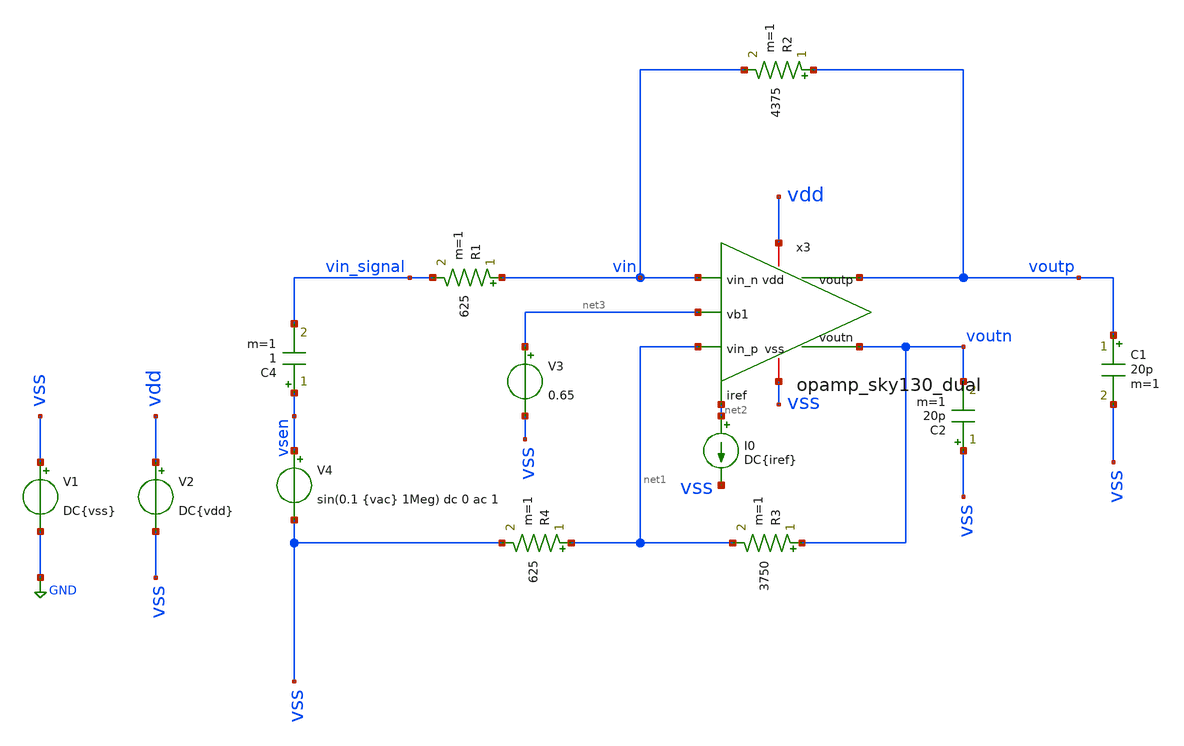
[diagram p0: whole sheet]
** sch_path: sch/tb_opamp_sky130_dual.sch
**.subckt tb_opamp_sky130_dual
V1 vss GND DC{vss}
V2 vdd vss DC{vdd}
V4 vsen vss sin(0.1 {vac} 1Meg) dc 0 ac 1
C4 vsen vin_signal 1 m=1
I0 net2 vss DC{iref}
R1 vin vin_signal 625 m=1
C1 voutp vss 20p m=1
R2 voutp vin 4375 m=1
C2 vss voutn 20p m=1
x3 vdd net2 vin net1 voutn voutp net3 vss opamp_sky130_dual
R3 voutn net1 3750 m=1
R4 net1 vss 625 m=1
V3 net3 vss 0.65
**** begin user architecture code




* Circuit Parameters
.param iref = 100u
.param vdd  = 1.8
.param vss  = 0.0
.param vac  = 0.1
.param vcm  = 0.7
.options TEMP = 65.0

* Include Models
*.lib ~/skywater_pdk/skywater-pdk/libraries/sky130_fd_pr/latest/models/corners/sky130.lib TT

* OP Parameters & Singals to save
.save all

*Simulations
.control


  reset
  tran 0.01u 11u
  setplot tran1
  plot v(vsen)  v(voutp) v(voutn)
  write tb_opamp_sky130_dual.raw

.endc

.end



** opencircuitdesign pdks install
.lib $::SKYWATER_MODELS/sky130.lib.spice tt


**** end user architecture code
**.ends

* expanding   symbol:  /home/alex/Desktop/EDA/TIA_IPN/sch/opamp_sky130_dual.sym # of pins=8
** sym_path: sch/opamp_sky130_dual.sym
** sch_path: sch/opamp_sky130_dual.sch
.subckt opamp_sky130_dual vdd iref vin_n vin_p voutn voutp vb1 vss
*.iopin vdd
*.iopin vss
*.ipin vin_n
*.ipin vin_p
*.ipin iref
*.opin voutn
*.opin voutp
*.ipin vb1
XM1 voe2 vin_n vp vp sky130_fd_pr__pfet_01v8 L=0.3 W=3 nf=1 ad='W * 0.29' as='W * 0.29' pd='2 * (W + 0.29)'
+ ps='2 * (W + 0.29)' nrd='0.29 / W' nrs='0.29 / W' sa=0 sb=0 sd=0 mult=200 m=200
XM2 voe1 vin_p vp vp sky130_fd_pr__pfet_01v8 L=0.3 W=3 nf=1 ad='W * 0.29' as='W * 0.29' pd='2 * (W + 0.29)'
+ ps='2 * (W + 0.29)' nrd='0.29 / W' nrs='0.29 / W' sa=0 sb=0 sd=0 mult=200 m=200
XM3 voe2 vb1 vss vss sky130_fd_pr__nfet_01v8 L=0.3 W=3 nf=1 ad='W * 0.29' as='W * 0.29' pd='2 * (W + 0.29)'
+ ps='2 * (W + 0.29)' nrd='0.29 / W' nrs='0.29 / W' sa=0 sb=0 sd=0 mult=30 m=30
XM4 voe1 vb1 vss vss sky130_fd_pr__nfet_01v8 L=0.3 W=3 nf=1 ad='W * 0.29' as='W * 0.29' pd='2 * (W + 0.29)'
+ ps='2 * (W + 0.29)' nrd='0.29 / W' nrs='0.29 / W' sa=0 sb=0 sd=0 mult=30 m=30
XM5 vp iref vdd vdd sky130_fd_pr__pfet_01v8 L=0.3 W=3 nf=1 ad='W * 0.29' as='W * 0.29' pd='2 * (W + 0.29)'
+ ps='2 * (W + 0.29)' nrd='0.29 / W' nrs='0.29 / W' sa=0 sb=0 sd=0 mult=30 m=30
XM7 voutn iref vdd vdd sky130_fd_pr__pfet_01v8 L=0.3 W=3 nf=1 ad='W * 0.29' as='W * 0.29' pd='2 * (W + 0.29)'
+ ps='2 * (W + 0.29)' nrd='0.29 / W' nrs='0.29 / W' sa=0 sb=0 sd=0 mult=150 m=150
XM8 iref iref vdd vdd sky130_fd_pr__pfet_01v8 L=0.3 W=3 nf=1 ad='W * 0.29' as='W * 0.29' pd='2 * (W + 0.29)'
+ ps='2 * (W + 0.29)' nrd='0.29 / W' nrs='0.29 / W' sa=0 sb=0 sd=0 mult=15 m=15
XM9 net1 vdd voe1 vss sky130_fd_pr__nfet_01v8 L=0.15 W=0.75 nf=1 ad='W * 0.29' as='W * 0.29' pd='2 * (W + 0.29)'
+ ps='2 * (W + 0.29)' nrd='0.29 / W' nrs='0.29 / W' sa=0 sb=0 sd=0 mult=6 m=6
XC1 net1 voutn sky130_fd_pr__cap_mim_m3_1 W=17.55 L=15 MF=6 m=6
XM6 voutn voe1 vss vss sky130_fd_pr__nfet_01v8 L=0.45 W=4.5 nf=1 ad='W * 0.29' as='W * 0.29' pd='2 * (W + 0.29)'
+ ps='2 * (W + 0.29)' nrd='0.29 / W' nrs='0.29 / W' sa=0 sb=0 sd=0 mult=150 m=150
XM10 voutp iref vdd vdd sky130_fd_pr__pfet_01v8 L=0.3 W=3 nf=1 ad='W * 0.29' as='W * 0.29' pd='2 * (W + 0.29)'
+ ps='2 * (W + 0.29)' nrd='0.29 / W' nrs='0.29 / W' sa=0 sb=0 sd=0 mult=150 m=150
XM11 voutp voe2 vss vss sky130_fd_pr__nfet_01v8 L=0.45 W=4.5 nf=1 ad='W * 0.29' as='W * 0.29' pd='2 * (W + 0.29)'
+ ps='2 * (W + 0.29)' nrd='0.29 / W' nrs='0.29 / W' sa=0 sb=0 sd=0 mult=150 m=150
XM12 net2 vdd voe2 vss sky130_fd_pr__nfet_01v8 L=0.15 W=0.75 nf=1 ad='W * 0.29' as='W * 0.29' pd='2 * (W + 0.29)'
+ ps='2 * (W + 0.29)' nrd='0.29 / W' nrs='0.29 / W' sa=0 sb=0 sd=0 mult=6 m=6
XC2 net2 voutp sky130_fd_pr__cap_mim_m3_1 W=17.55 L=15 MF=6 m=6
.ends

.GLOBAL GND
.end
